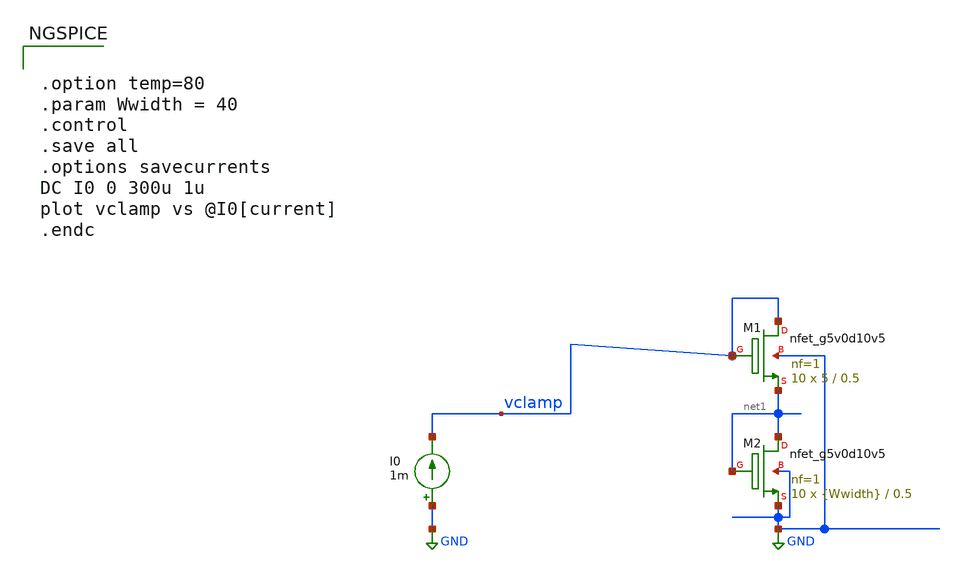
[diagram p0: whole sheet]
** sch_path: images/foss-asic-tools/addons/examples/open-pmic/characterization/NMOS_diode_test.sch
**.subckt NMOS_diode_test
I0 GND vclamp 1m
XM2 net1 net1 GND GND sky130_fd_pr__nfet_g5v0d10v5 L=0.5 W={Wwidth} nf=1 ad='int((nf+1)/2) * W/nf * 0.29'
+ as='int((nf+2)/2) * W/nf * 0.29' pd='2*int((nf+1)/2) * (W/nf + 0.29)' ps='2*int((nf+2)/2) * (W/nf + 0.29)'
+ nrd='0.29 / W' nrs='0.29 / W' sa=0 sb=0 sd=0 mult=10 m=10
XM1 vclamp vclamp net1 GND sky130_fd_pr__nfet_g5v0d10v5 L=0.5 W=5 nf=1 ad='int((nf+1)/2) * W/nf * 0.29'
+ as='int((nf+2)/2) * W/nf * 0.29' pd='2*int((nf+1)/2) * (W/nf + 0.29)' ps='2*int((nf+2)/2) * (W/nf + 0.29)'
+ nrd='0.29 / W' nrs='0.29 / W' sa=0 sb=0 sd=0 mult=10 m=10
**** begin user architecture code


.option temp=80
.param Wwidth = 40
.control
.save all
.options savecurrents
DC I0 0 300u 1u
plot vclamp vs @I0[current]
.endc



.lib $::SKYWATER_MODELS/models/sky130.lib.spice ss
.option wnflag=1

**** end user architecture code
**.ends
.GLOBAL GND
.end
